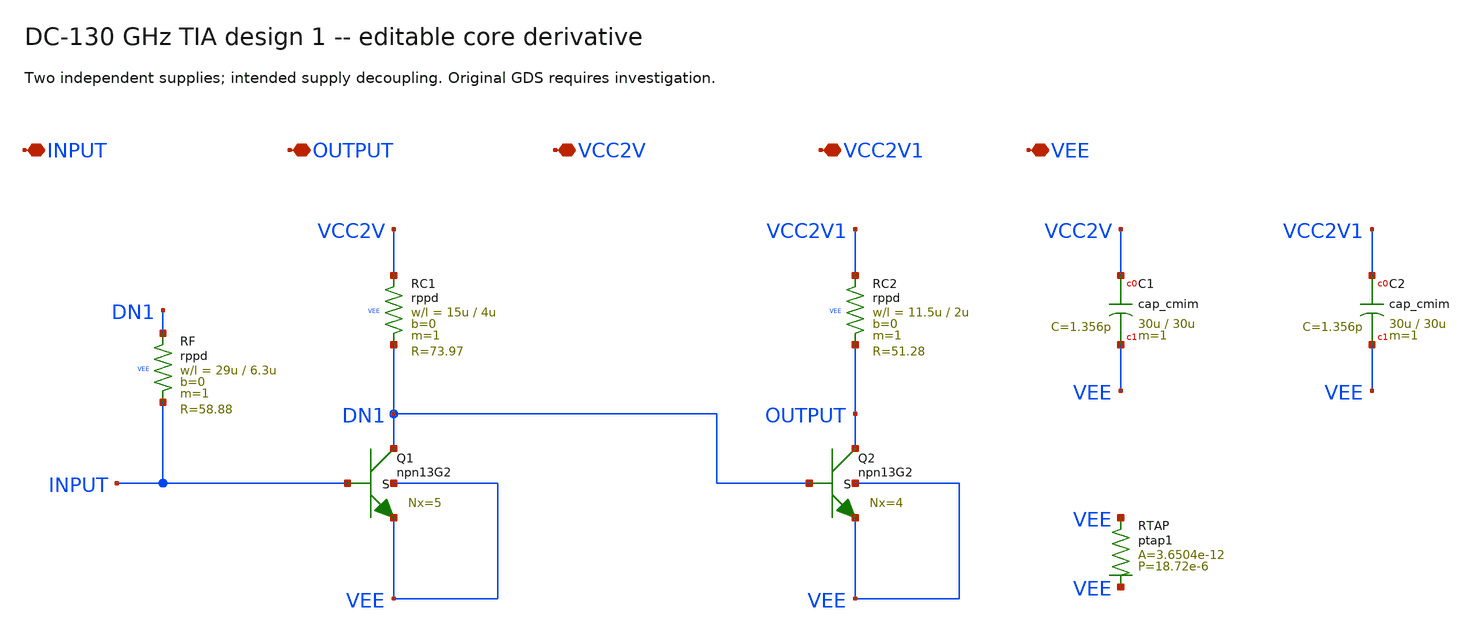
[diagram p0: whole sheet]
** sch_path: tasks/TO_Apr2025/cases/DC_to_130_GHz_TIA.design_1/source/FMD_QNC_03a_TIA_1.sch
* SPDX-License-Identifier: Apache-2.0
**.subckt FMD_QNC_03a_TIA_1 INPUT OUTPUT VCC2V VCC2V1 VEE
*.iopin INPUT
*.iopin OUTPUT
*.iopin VCC2V
*.iopin VCC2V1
*.iopin VEE
XQ1 DN1 INPUT VEE VEE npn13G2 Nx=5 mm_ok=0
XQ2 OUTPUT DN1 VEE VEE npn13G2 Nx=4 mm_ok=0
XRC1 VCC2V DN1 VEE rppd w=15u l=4u m=1 b=0 mm_ok=0
XRC2 VCC2V1 OUTPUT VEE rppd w=11.5u l=2u m=1 b=0 mm_ok=0
XRF DN1 INPUT VEE rppd w=29u l=6.3u m=1 b=0 mm_ok=0
XC1 VCC2V VEE cap_cmim w=30u l=30u m=1 mm_ok=0
XC2 VCC2V1 VEE cap_cmim w=30u l=30u m=1 mm_ok=0
XRTAP VEE VEE ptap1 a=3.6504e-12 p=18.72e-6 r=43.81
**.ends
.end
